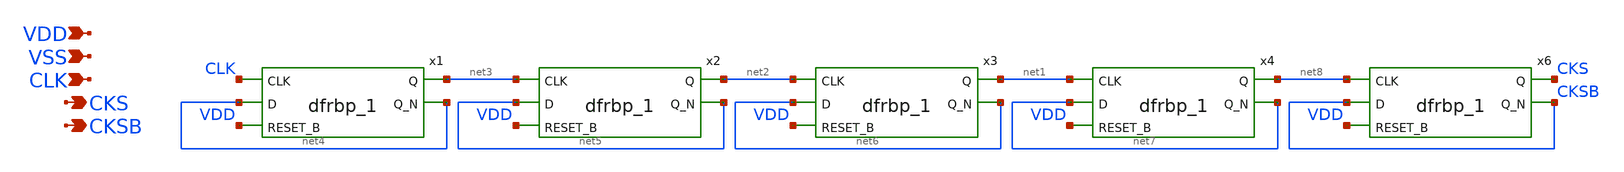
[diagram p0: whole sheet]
** sch_path: xschem/freq_div.sch
**.subckt freq_div VDD VSS CLK CKS CKSB
*.ipin VDD
*.ipin VSS
*.ipin CLK
*.opin CKS
*.opin CKSB
x1 CLK net4 VDD VSS VSS VDD VDD net3 net4 sky130_fd_sc_hd__dfrbp_1
x2 net3 net5 VDD VSS VSS VDD VDD net2 net5 sky130_fd_sc_hd__dfrbp_1
x3 net2 net6 VDD VSS VSS VDD VDD net1 net6 sky130_fd_sc_hd__dfrbp_1
x4 net1 net7 VDD VSS VSS VDD VDD net8 net7 sky130_fd_sc_hd__dfrbp_1
x6 net8 CKSB VDD VSS VSS VDD VDD CKS CKSB sky130_fd_sc_hd__dfrbp_1
**.ends
.end
